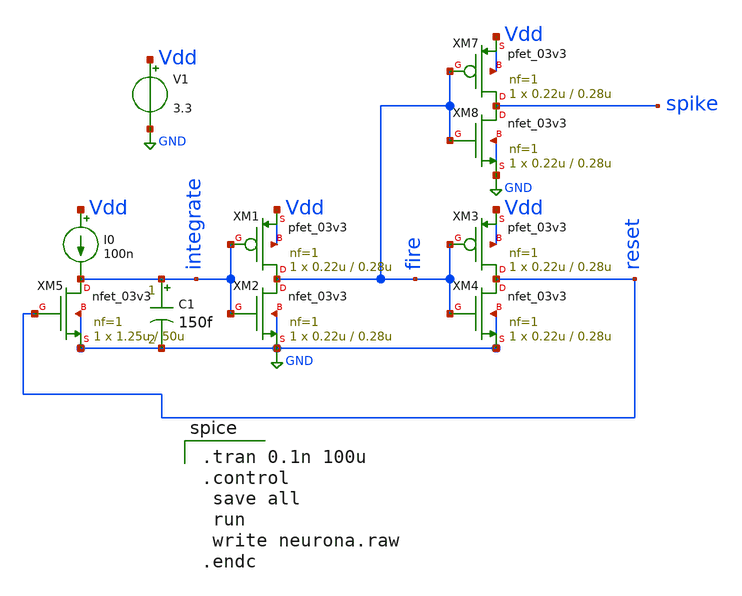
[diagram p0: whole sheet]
** sch_path: sch/lif/neurona.sch
**.subckt neurona
XM1 fire integrate Vdd Vdd pfet_03v3 L=0.28u W=0.22u nf=1 ad='int((nf+1)/2) * W/nf * 0.18u' as='int((nf+2)/2) * W/nf * 0.18u'
+ pd='2*int((nf+1)/2) * (W/nf + 0.18u)' ps='2*int((nf+2)/2) * (W/nf + 0.18u)' nrd='0.18u / W' nrs='0.18u / W'
+ sa=0 sb=0 sd=0 m=1
XM2 fire integrate GND GND nfet_03v3 L=0.28u W=0.22u nf=1 ad='int((nf+1)/2) * W/nf * 0.18u' as='int((nf+2)/2) * W/nf * 0.18u'
+ pd='2*int((nf+1)/2) * (W/nf + 0.18u)' ps='2*int((nf+2)/2) * (W/nf + 0.18u)' nrd='0.18u / W' nrs='0.18u / W'
+ sa=0 sb=0 sd=0 m=1
XM3 reset fire Vdd Vdd pfet_03v3 L=0.28u W=0.22u nf=1 ad='int((nf+1)/2) * W/nf * 0.18u' as='int((nf+2)/2) * W/nf * 0.18u'
+ pd='2*int((nf+1)/2) * (W/nf + 0.18u)' ps='2*int((nf+2)/2) * (W/nf + 0.18u)' nrd='0.18u / W' nrs='0.18u / W'
+ sa=0 sb=0 sd=0 m=1
XM4 reset fire GND GND nfet_03v3 L=0.28u W=0.22u nf=1 ad='int((nf+1)/2) * W/nf * 0.18u' as='int((nf+2)/2) * W/nf * 0.18u'
+ pd='2*int((nf+1)/2) * (W/nf + 0.18u)' ps='2*int((nf+2)/2) * (W/nf + 0.18u)' nrd='0.18u / W' nrs='0.18u / W'
+ sa=0 sb=0 sd=0 m=1
XM7 spike fire Vdd Vdd pfet_03v3 L=0.28u W=0.22u nf=1 ad='int((nf+1)/2) * W/nf * 0.18u' as='int((nf+2)/2) * W/nf * 0.18u'
+ pd='2*int((nf+1)/2) * (W/nf + 0.18u)' ps='2*int((nf+2)/2) * (W/nf + 0.18u)' nrd='0.18u / W' nrs='0.18u / W'
+ sa=0 sb=0 sd=0 m=1
XM8 spike fire GND GND nfet_03v3 L=0.28u W=0.22u nf=1 ad='int((nf+1)/2) * W/nf * 0.18u' as='int((nf+2)/2) * W/nf * 0.18u'
+ pd='2*int((nf+1)/2) * (W/nf + 0.18u)' ps='2*int((nf+2)/2) * (W/nf + 0.18u)' nrd='0.18u / W' nrs='0.18u / W'
+ sa=0 sb=0 sd=0 m=1
XM5 integrate reset GND GND nfet_03v3 L=50u W=1.25u nf=1 ad='int((nf+1)/2) * W/nf * 0.18u' as='int((nf+2)/2) * W/nf * 0.18u'
+ pd='2*int((nf+1)/2) * (W/nf + 0.18u)' ps='2*int((nf+2)/2) * (W/nf + 0.18u)' nrd='0.18u / W' nrs='0.18u / W'
+ sa=0 sb=0 sd=0 m=1
V1 Vdd GND 3.3
I0 Vdd integrate 100n
C1 integrate GND 150f m=1
**** begin user architecture code

.include $::180MCU_MODELS/design.ngspice
.lib $::180MCU_MODELS/sm141064.ngspice typical


.tran 0.1n 100u
.control
 save all
 run
 write neurona.raw
.endc

**** end user architecture code
**.ends
.GLOBAL GND
.end
